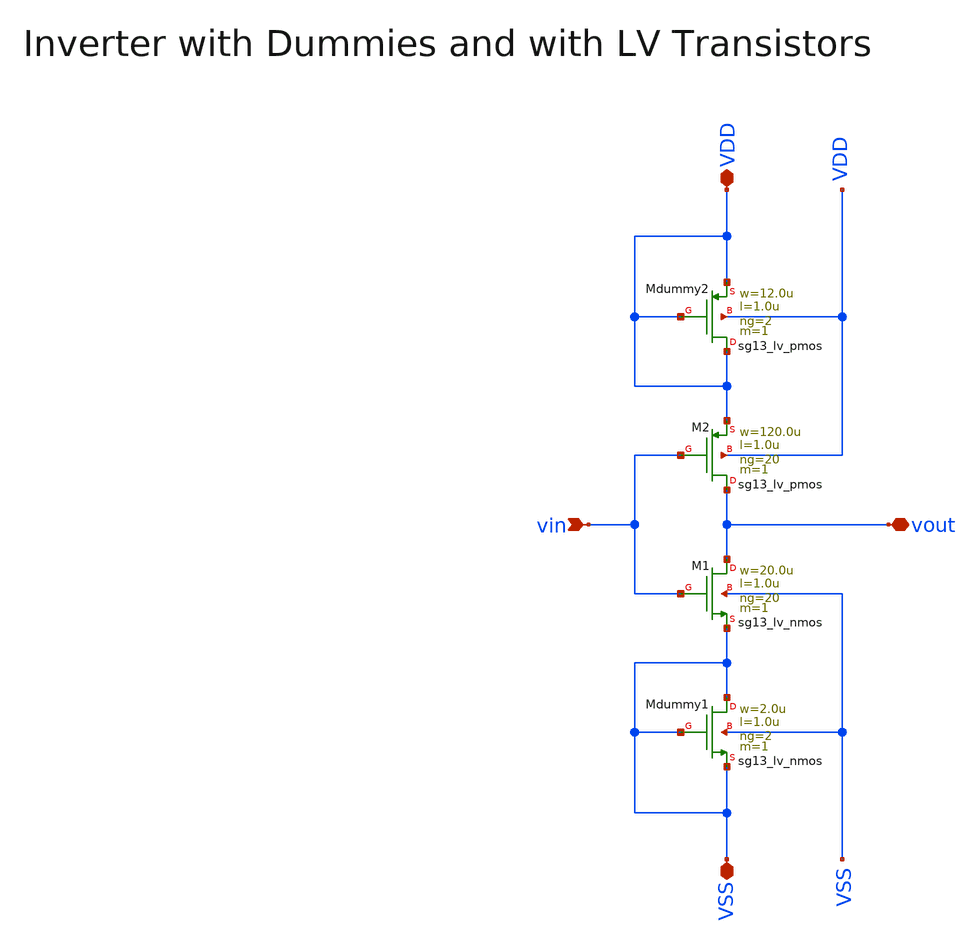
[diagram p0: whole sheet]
** sch_path: macros/heichips26_analog_project/macros/inverter/schematic/xschem/inverter.sch
**.subckt inverter vin VDD VSS vout
*.ipin vin
*.iopin VDD
*.iopin VSS
*.iopin vout
XMdummy1 VSS VSS VSS VSS sg13_lv_nmos w=2.0u l=1.0u ng=2 m=1 mm_ok=1
XMdummy2 VDD VDD VDD VDD sg13_lv_pmos w=12.0u l=1.0u ng=2 m=1 mm_ok=1
XM1 vout vin VSS VSS sg13_lv_nmos w=20.0u l=1.0u ng=20 m=1 mm_ok=1
XM2 vout vin VDD VDD sg13_lv_pmos w=120.0u l=1.0u ng=20 m=1 mm_ok=1
**.ends
.end
